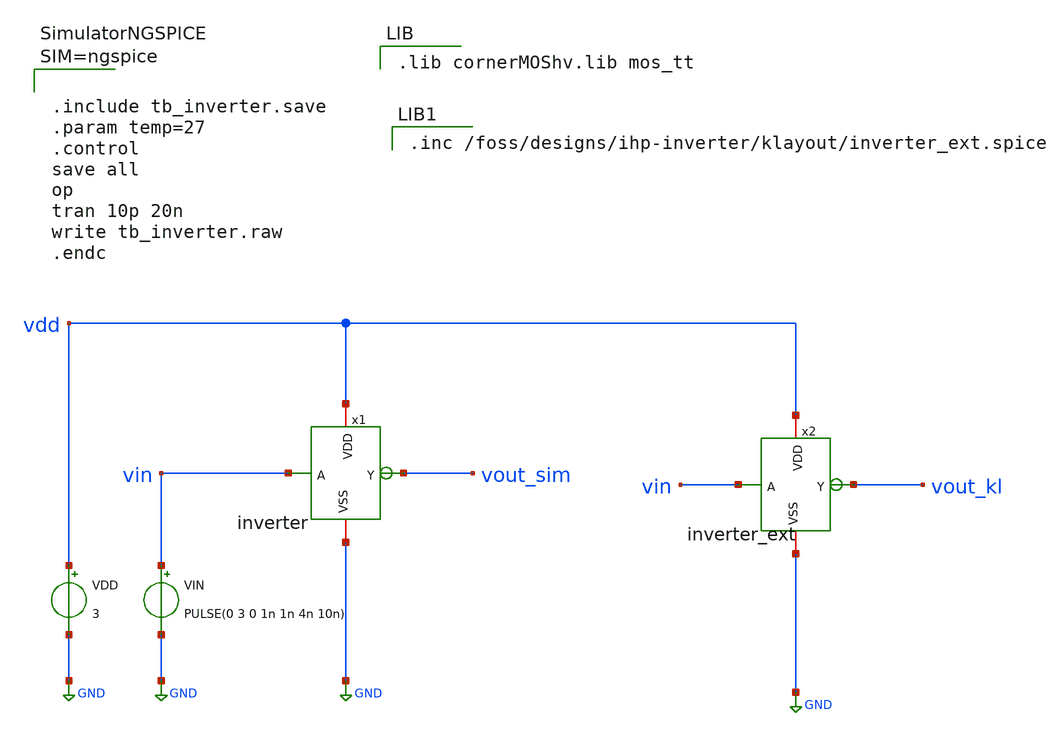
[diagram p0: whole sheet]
** sch_path: xschem/tb_inverter.sch
**.subckt tb_inverter
VIN vin GND PULSE(0 3 0 1n 1n 4n 10n)
VDD vdd GND 3
x1 vdd vin vout_sim GND inverter
x2 vdd vin vout_kl GND inverter_ext
**** begin user architecture code

.lib cornerMOShv.lib mos_tt





.include tb_inverter.save
.param temp=27
.control
save all
op
tran 10p 20n
write tb_inverter.raw
.endc




.inc /foss/designs/ihp-inverter/klayout/inverter_ext.spice

**** end user architecture code
**.ends

* expanding   symbol:  inverter.sym # of pins=4
** sym_path: xschem/inverter.sym
** sch_path: xschem/inverter.sch
.subckt inverter VDD A Y VSS
*.ipin A
*.opin Y
*.iopin VDD
*.iopin VSS
XM1 Y A VSS VSS sg13_hv_nmos w=0.3u l=0.45u ng=1 m=1 mm_ok=1
XM2 Y A VDD VDD sg13_hv_pmos w=0.3u l=0.45u ng=1 m=1 mm_ok=1
.ends

.GLOBAL GND
.end
